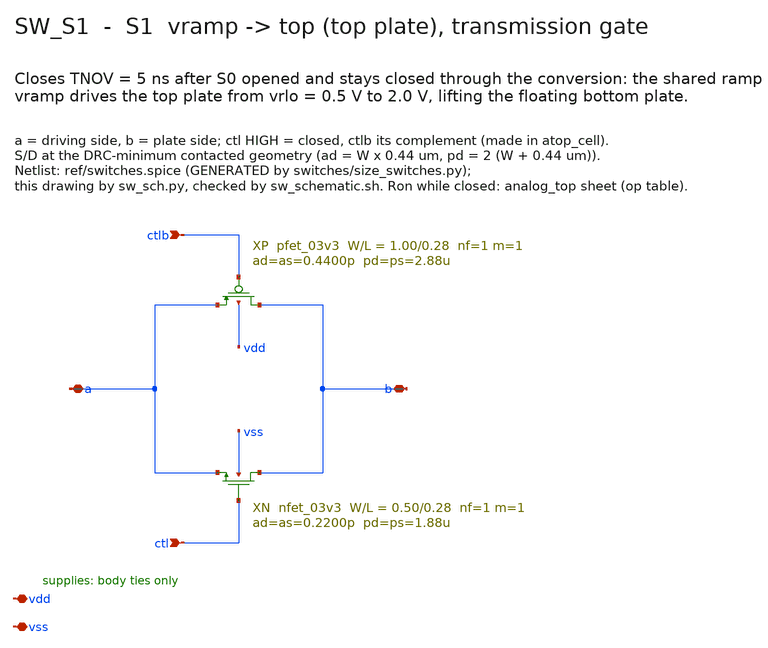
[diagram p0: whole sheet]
** sch_path: mixed_signal/Analog_top/sw_s1.sch
**.subckt sw_s1 ctl ctlb a b vdd vss
*.ipin ctl
*.ipin ctlb
*.iopin a
*.iopin b
*.iopin vdd
*.iopin vss
XN b ctl a vss nfet_03v3 L=0.28u W=0.50u nf=1 m=1 ad=0.2200p as=0.2200p pd=1.88u ps=1.88u
XP b ctlb a vdd pfet_03v3 L=0.28u W=1.00u nf=1 m=1 ad=0.4400p as=0.4400p pd=2.88u ps=2.88u
**.ends
.end
